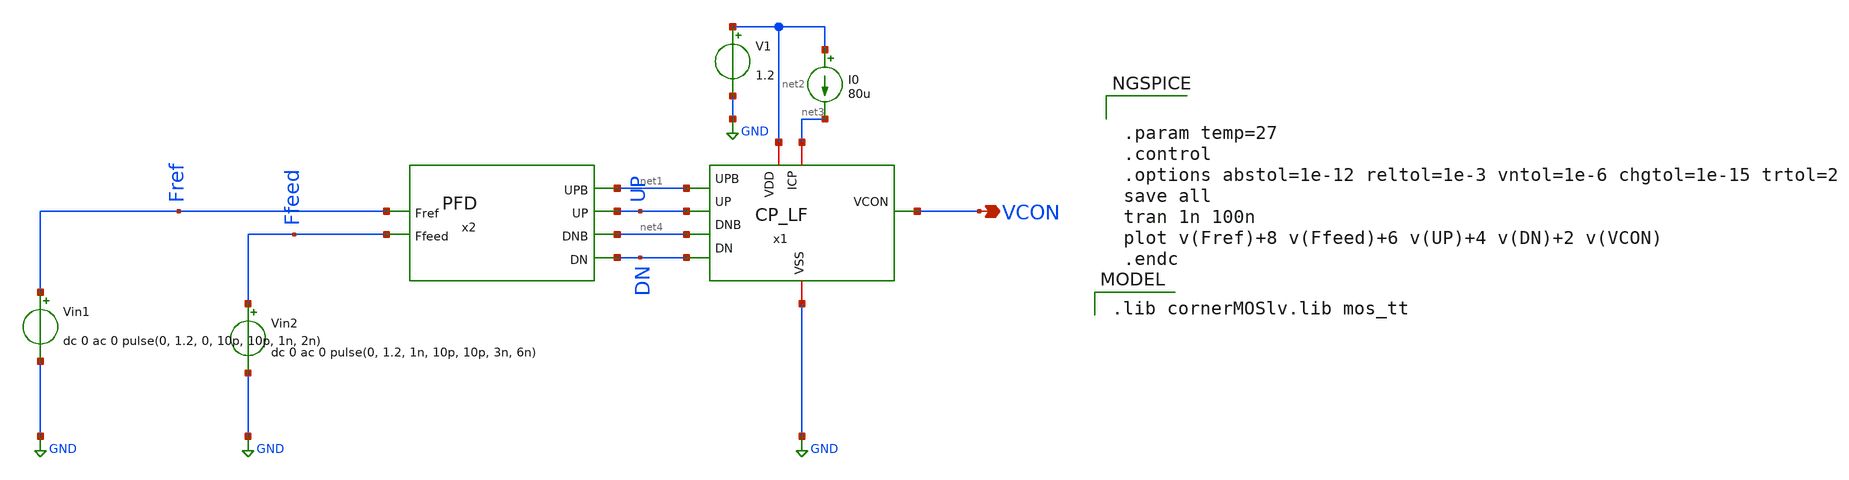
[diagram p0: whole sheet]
** sch_path: Team 1 Design/design_data/xschem/CP_LF/CP_LF_tb.sch
**.subckt CP_LF_tb VCON
*.opin VCON
Vin1 Fref GND dc 0 ac 0 pulse(0, 1.2, 0, 10p, 10p, 1n, 2n)
Vin2 Ffeed GND dc 0 ac 0 pulse(0, 1.2, 1n, 10p, 10p, 3n, 6n)
V1 net2 GND 1.2
I0 net2 net3 80u
x1 net2 net3 GND net1 UP VCON net4 DN CP_LF
x2 Fref UP net1 DN net4 Ffeed PFD
**** begin user architecture code
 .lib cornerMOSlv.lib mos_tt



.param temp=27
.control
.options abstol=1e-12 reltol=1e-3 vntol=1e-6 chgtol=1e-15 trtol=2
save all
tran 1n 100n
plot v(Fref)+8 v(Ffeed)+6 v(UP)+4 v(DN)+2 v(VCON)
.endc


**** end user architecture code
**.ends
.GLOBAL GND
.end
